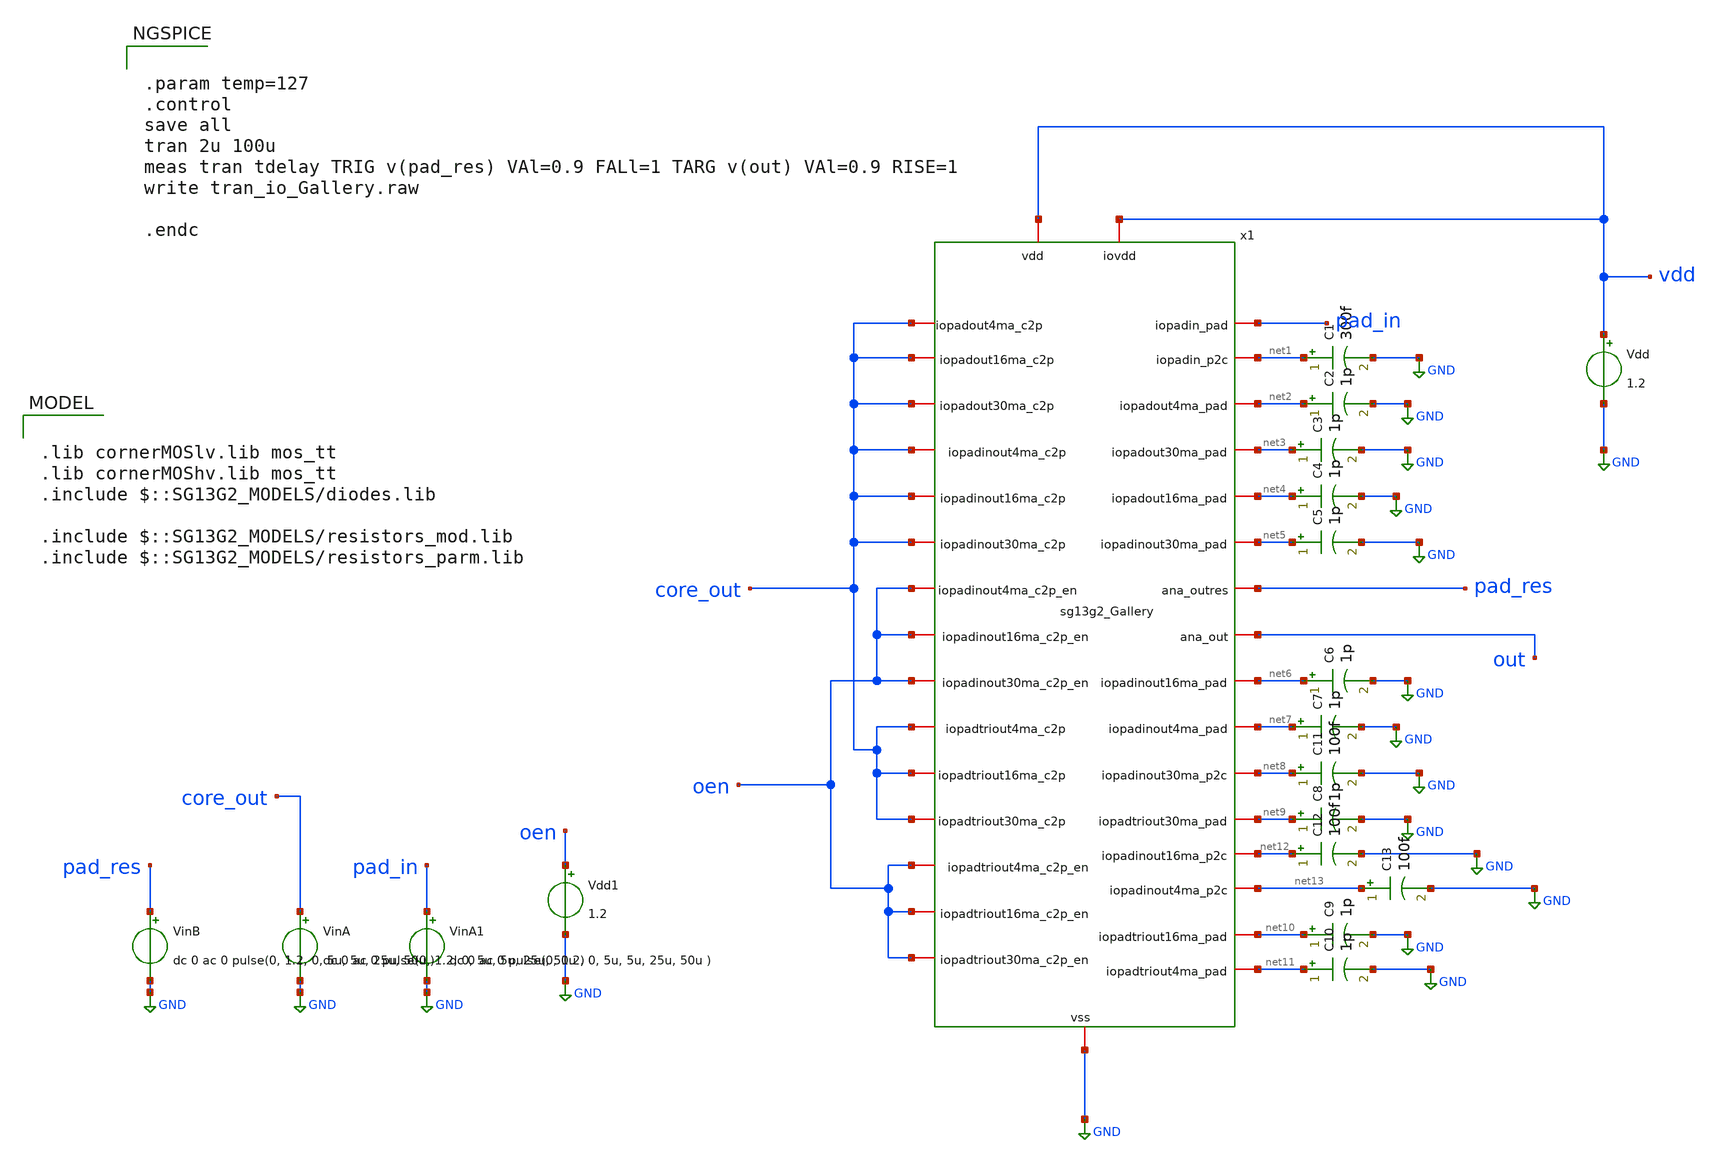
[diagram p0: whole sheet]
** sch_path: ihp-sg13g2/libs.ref/sg13g2_io/xschem/io_testbench/sg13g2_io_Gallery_tb.sch
* Copyright 2023 IHP PDK Authors
**.subckt sg13g2_io_Gallery_tb
VinA core_out GND dc 0 ac 0 pulse(0, 1.2, 0, 5u, 5u, 25u, 50u )
Vdd vdd GND 1.2
VinB pad_res GND dc 0 ac 0 pulse(0, 1.2, 0, 5u, 5u, 25u, 50u )
x1 pad_in core_out core_out core_out net1 net2 net3 vdd vdd net4 out pad_res oen core_out oen oen
+ oen net5 net6 core_out oen net7 core_out core_out net8 core_out net9 net12 net13 core_out oen net10
+ net11 GND sg13g2_Gallery
C1 net1 GND 300f m=1
C2 net2 GND 1p m=1
C3 net3 GND 1p m=1
C4 net4 GND 1p m=1
C5 net5 GND 1p m=1
C6 net6 GND 1p m=1
C7 net7 GND 1p m=1
C8 net9 GND 1p m=1
C9 net10 GND 1p m=1
C10 net11 GND 1p m=1
C11 net8 GND 100f m=1
C12 net12 GND 100f m=1
C13 net13 GND 100f m=1
VinA1 pad_in GND dc 0 ac 0 pulse(0, 1.2, 0, 5u, 5u, 25u, 50u )
Vdd1 oen GND 1.2
**** begin user architecture code

.lib cornerMOSlv.lib mos_tt
.lib cornerMOShv.lib mos_tt
.include $::SG13G2_MODELS/diodes.lib

.include $::SG13G2_MODELS/resistors_mod.lib
.include $::SG13G2_MODELS/resistors_parm.lib






.param temp=127
.control
save all
tran 2u 100u
meas tran tdelay TRIG v(pad_res) VAl=0.9 FALl=1 TARG v(out) VAl=0.9 RISE=1
write tran_io_Gallery.raw

.endc


**** end user architecture code
**.ends
.GLOBAL GND
.end
